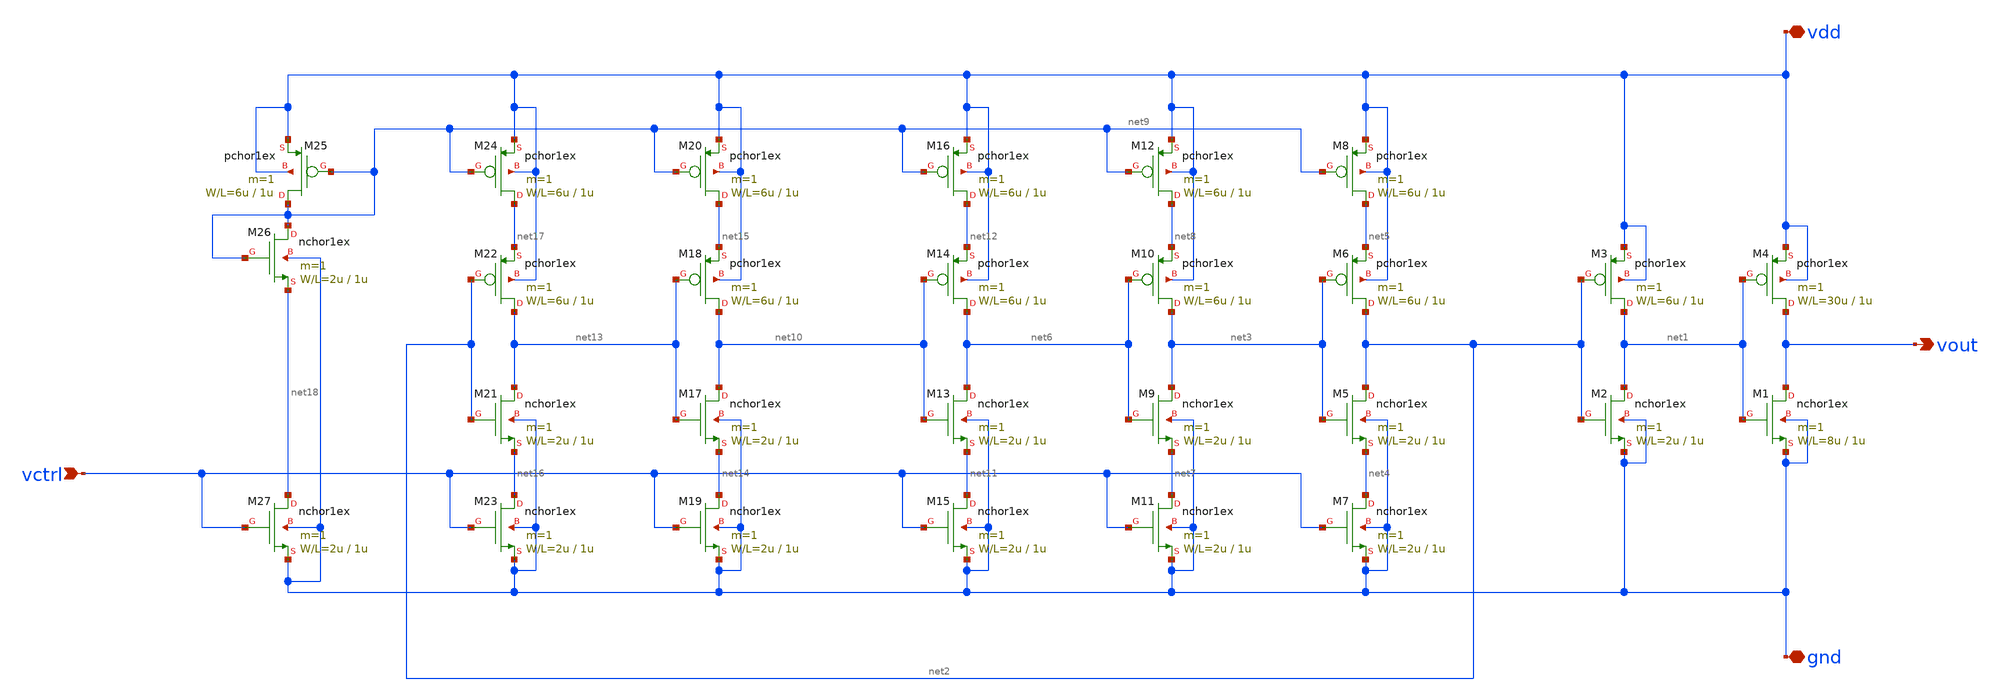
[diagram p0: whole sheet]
** sch_path: member_project/Sinby/vco_osc5.sch
**.subckt vco_osc5 vdd gnd vout vctrl
*.iopin vdd
*.iopin gnd
*.opin vout
*.ipin vctrl
M1 vout net1 gnd gnd nchor1ex L=1u W=8u m=1
M4 vout net1 vdd vdd pchor1ex L=1u W=30u m=1
M2 net1 net2 gnd gnd nchor1ex L=1u W=2u m=1
M3 net1 net2 vdd vdd pchor1ex L=1u W=6u m=1
M5 net2 net3 net4 gnd nchor1ex L=1u W=2u m=1
M6 net2 net3 net5 vdd pchor1ex L=1u W=6u m=1
M7 net4 vctrl gnd gnd nchor1ex L=1u W=2u m=1
M8 net5 net9 vdd vdd pchor1ex L=1u W=6u m=1
M9 net3 net6 net7 gnd nchor1ex L=1u W=2u m=1
M10 net3 net6 net8 vdd pchor1ex L=1u W=6u m=1
M11 net7 vctrl gnd gnd nchor1ex L=1u W=2u m=1
M12 net8 net9 vdd vdd pchor1ex L=1u W=6u m=1
M13 net6 net10 net11 gnd nchor1ex L=1u W=2u m=1
M14 net6 net10 net12 vdd pchor1ex L=1u W=6u m=1
M15 net11 vctrl gnd gnd nchor1ex L=1u W=2u m=1
M16 net12 net9 vdd vdd pchor1ex L=1u W=6u m=1
M17 net10 net13 net14 gnd nchor1ex L=1u W=2u m=1
M18 net10 net13 net15 vdd pchor1ex L=1u W=6u m=1
M19 net14 vctrl gnd gnd nchor1ex L=1u W=2u m=1
M20 net15 net9 vdd vdd pchor1ex L=1u W=6u m=1
M21 net13 net2 net16 gnd nchor1ex L=1u W=2u m=1
M22 net13 net2 net17 vdd pchor1ex L=1u W=6u m=1
M23 net16 vctrl gnd gnd nchor1ex L=1u W=2u m=1
M24 net17 net9 vdd vdd pchor1ex L=1u W=6u m=1
M25 net9 net9 vdd vdd pchor1ex L=1u W=6u m=1
M26 net9 net9 net18 gnd nchor1ex L=1u W=2u m=1
M27 net18 vctrl gnd gnd nchor1ex L=1u W=2u m=1
**.ends
.end
